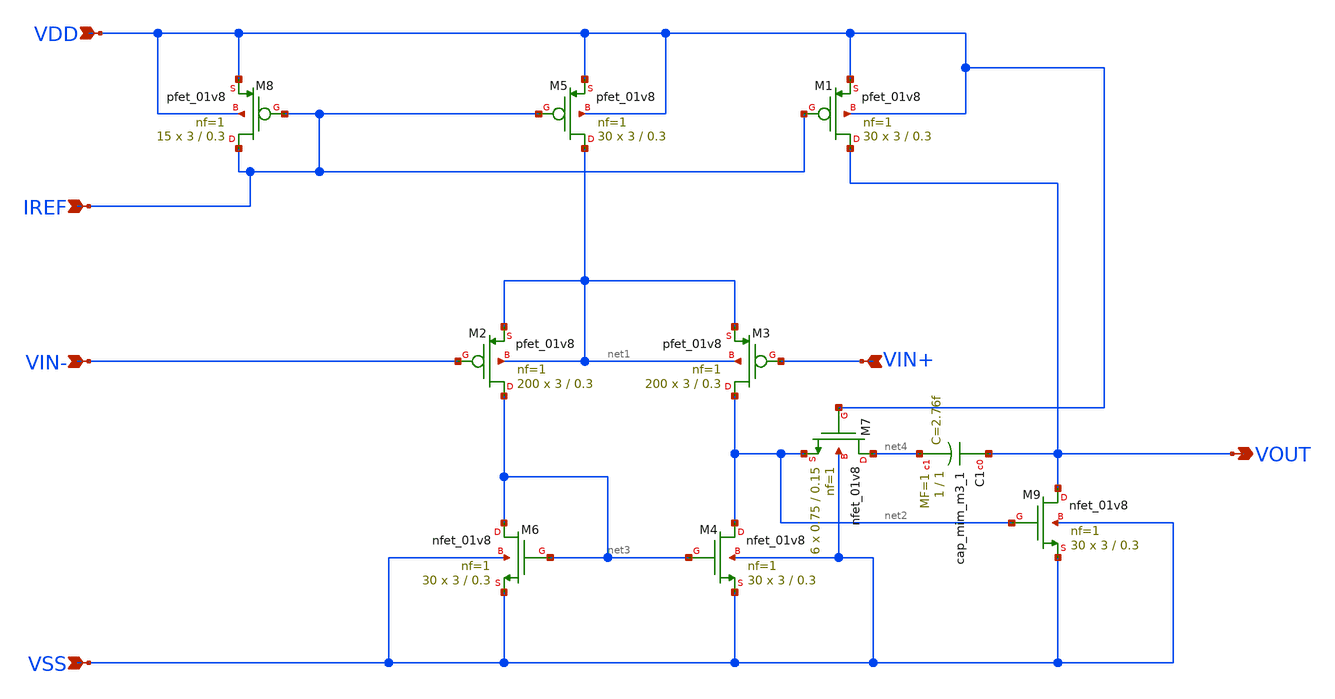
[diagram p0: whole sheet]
** sch_path: OPAMP_1.sch
**.subckt OPAMP_1 VIN- IREF VIN+ VOUT VDD VSS
*.ipin VIN-
*.ipin IREF
*.ipin VIN+
*.opin VOUT
*.ipin VDD
*.ipin VSS
XM8 IREF IREF VDD VDD sky130_fd_pr__pfet_01v8 L=0.3 W=3 nf=1 ad='int((nf+1)/2) * W/nf * 0.29' as='int((nf+2)/2) * W/nf * 0.29'
+ pd='2*int((nf+1)/2) * (W/nf + 0.29)' ps='2*int((nf+2)/2) * (W/nf + 0.29)' nrd='0.29 / W' nrs='0.29 / W'
+ sa=0 sb=0 sd=0 mult=15 m=15
XM5 net1 IREF VDD VDD sky130_fd_pr__pfet_01v8 L=0.3 W=3 nf=1 ad='int((nf+1)/2) * W/nf * 0.29' as='int((nf+2)/2) * W/nf * 0.29'
+ pd='2*int((nf+1)/2) * (W/nf + 0.29)' ps='2*int((nf+2)/2) * (W/nf + 0.29)' nrd='0.29 / W' nrs='0.29 / W'
+ sa=0 sb=0 sd=0 mult=30 m=30
XM1 VOUT IREF VDD VDD sky130_fd_pr__pfet_01v8 L=0.3 W=3 nf=1 ad='int((nf+1)/2) * W/nf * 0.29' as='int((nf+2)/2) * W/nf * 0.29'
+ pd='2*int((nf+1)/2) * (W/nf + 0.29)' ps='2*int((nf+2)/2) * (W/nf + 0.29)' nrd='0.29 / W' nrs='0.29 / W'
+ sa=0 sb=0 sd=0 mult=30 m=30
XM2 net3 VIN- net1 net1 sky130_fd_pr__pfet_01v8 L=0.3 W=3 nf=1 ad='int((nf+1)/2) * W/nf * 0.29' as='int((nf+2)/2) * W/nf * 0.29'
+ pd='2*int((nf+1)/2) * (W/nf + 0.29)' ps='2*int((nf+2)/2) * (W/nf + 0.29)' nrd='0.29 / W' nrs='0.29 / W'
+ sa=0 sb=0 sd=0 mult=200 m=200
XM3 net2 VIN+ net1 net1 sky130_fd_pr__pfet_01v8 L=0.3 W=3 nf=1 ad='int((nf+1)/2) * W/nf * 0.29' as='int((nf+2)/2) * W/nf * 0.29'
+ pd='2*int((nf+1)/2) * (W/nf + 0.29)' ps='2*int((nf+2)/2) * (W/nf + 0.29)' nrd='0.29 / W' nrs='0.29 / W'
+ sa=0 sb=0 sd=0 mult=200 m=200
XM4 net2 net3 VSS VSS sky130_fd_pr__nfet_01v8 L=0.3 W=3 nf=1 ad='int((nf+1)/2) * W/nf * 0.29' as='int((nf+2)/2) * W/nf * 0.29'
+ pd='2*int((nf+1)/2) * (W/nf + 0.29)' ps='2*int((nf+2)/2) * (W/nf + 0.29)' nrd='0.29 / W' nrs='0.29 / W'
+ sa=0 sb=0 sd=0 mult=30 m=30
XM6 net3 net3 VSS VSS sky130_fd_pr__nfet_01v8 L=0.3 W=3 nf=1 ad='int((nf+1)/2) * W/nf * 0.29' as='int((nf+2)/2) * W/nf * 0.29'
+ pd='2*int((nf+1)/2) * (W/nf + 0.29)' ps='2*int((nf+2)/2) * (W/nf + 0.29)' nrd='0.29 / W' nrs='0.29 / W'
+ sa=0 sb=0 sd=0 mult=30 m=30
XM7 net4 VDD net2 VSS sky130_fd_pr__nfet_01v8 L=0.15 W=0.75 nf=1 ad='int((nf+1)/2) * W/nf * 0.29' as='int((nf+2)/2) * W/nf * 0.29'
+ pd='2*int((nf+1)/2) * (W/nf + 0.29)' ps='2*int((nf+2)/2) * (W/nf + 0.29)' nrd='0.29 / W' nrs='0.29 / W'
+ sa=0 sb=0 sd=0 mult=6 m=6
XM9 VOUT net2 VSS VSS sky130_fd_pr__nfet_01v8 L=0.3 W=3 nf=1 ad='int((nf+1)/2) * W/nf * 0.29' as='int((nf+2)/2) * W/nf * 0.29'
+ pd='2*int((nf+1)/2) * (W/nf + 0.29)' ps='2*int((nf+2)/2) * (W/nf + 0.29)' nrd='0.29 / W' nrs='0.29 / W'
+ sa=0 sb=0 sd=0 mult=30 m=30
XC1 VOUT net4 sky130_fd_pr__cap_mim_m3_1 W=1 L=1 MF=1 m=1
**.ends
.end
